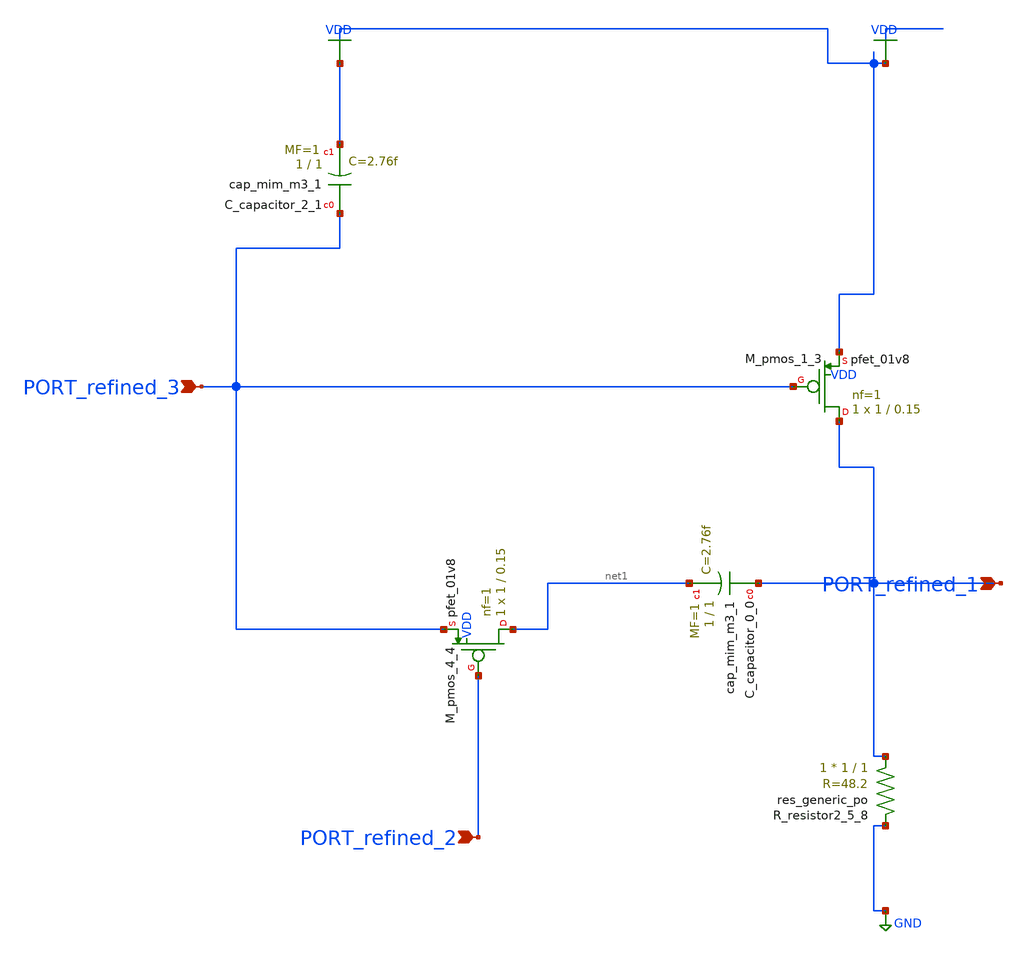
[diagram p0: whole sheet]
** sch_path: schematics/AMSNet/725.sch
**.subckt 725 PORT_refined_1 PORT_refined_2 PORT_refined_3
*.ipin PORT_refined_1
*.ipin PORT_refined_2
*.ipin PORT_refined_3
XC_capacitor_0_0 PORT_refined_1 net1 sky130_fd_pr__cap_mim_m3_1 W=1 L=1 MF=1 m=1
XC_capacitor_2_1 PORT_refined_3 VDD sky130_fd_pr__cap_mim_m3_1 W=1 L=1 MF=1 m=1
XM_pmos_1_3 PORT_refined_1 PORT_refined_3 VDD VDD sky130_fd_pr__pfet_01v8 L=0.15 W=1 nf=1 ad='int((1 + 1)/2) * 1 / 1 * 0.29'
+ as='int((1 + 2)/2) * 1 / 1 * 0.29' pd='2*int((1 + 1)/2) * (1 / 1 + 0.29)' ps='2*int((1 + 2)/2) * (1 / 1 + 0.29)'
+ nrd='0.29 / 1 ' nrs='0.29 / 1 ' sa=0 sb=0 sd=0 mult=1 m=1
XM_pmos_4_4 net1 PORT_refined_2 PORT_refined_3 VDD sky130_fd_pr__pfet_01v8 L=0.15 W=1 nf=1 ad='int((1 + 1)/2) * 1 / 1 * 0.29'
+ as='int((1 + 2)/2) * 1 / 1 * 0.29' pd='2*int((1 + 1)/2) * (1 / 1 + 0.29)' ps='2*int((1 + 2)/2) * (1 / 1 + 0.29)'
+ nrd='0.29 / 1 ' nrs='0.29 / 1 ' sa=0 sb=0 sd=0 mult=1 m=1
XR_resistor2_5_8 PORT_refined_1 GND sky130_fd_pr__res_generic_po W=1 L=1 m=1
**.ends
.GLOBAL GND
.GLOBAL VDD
.end
